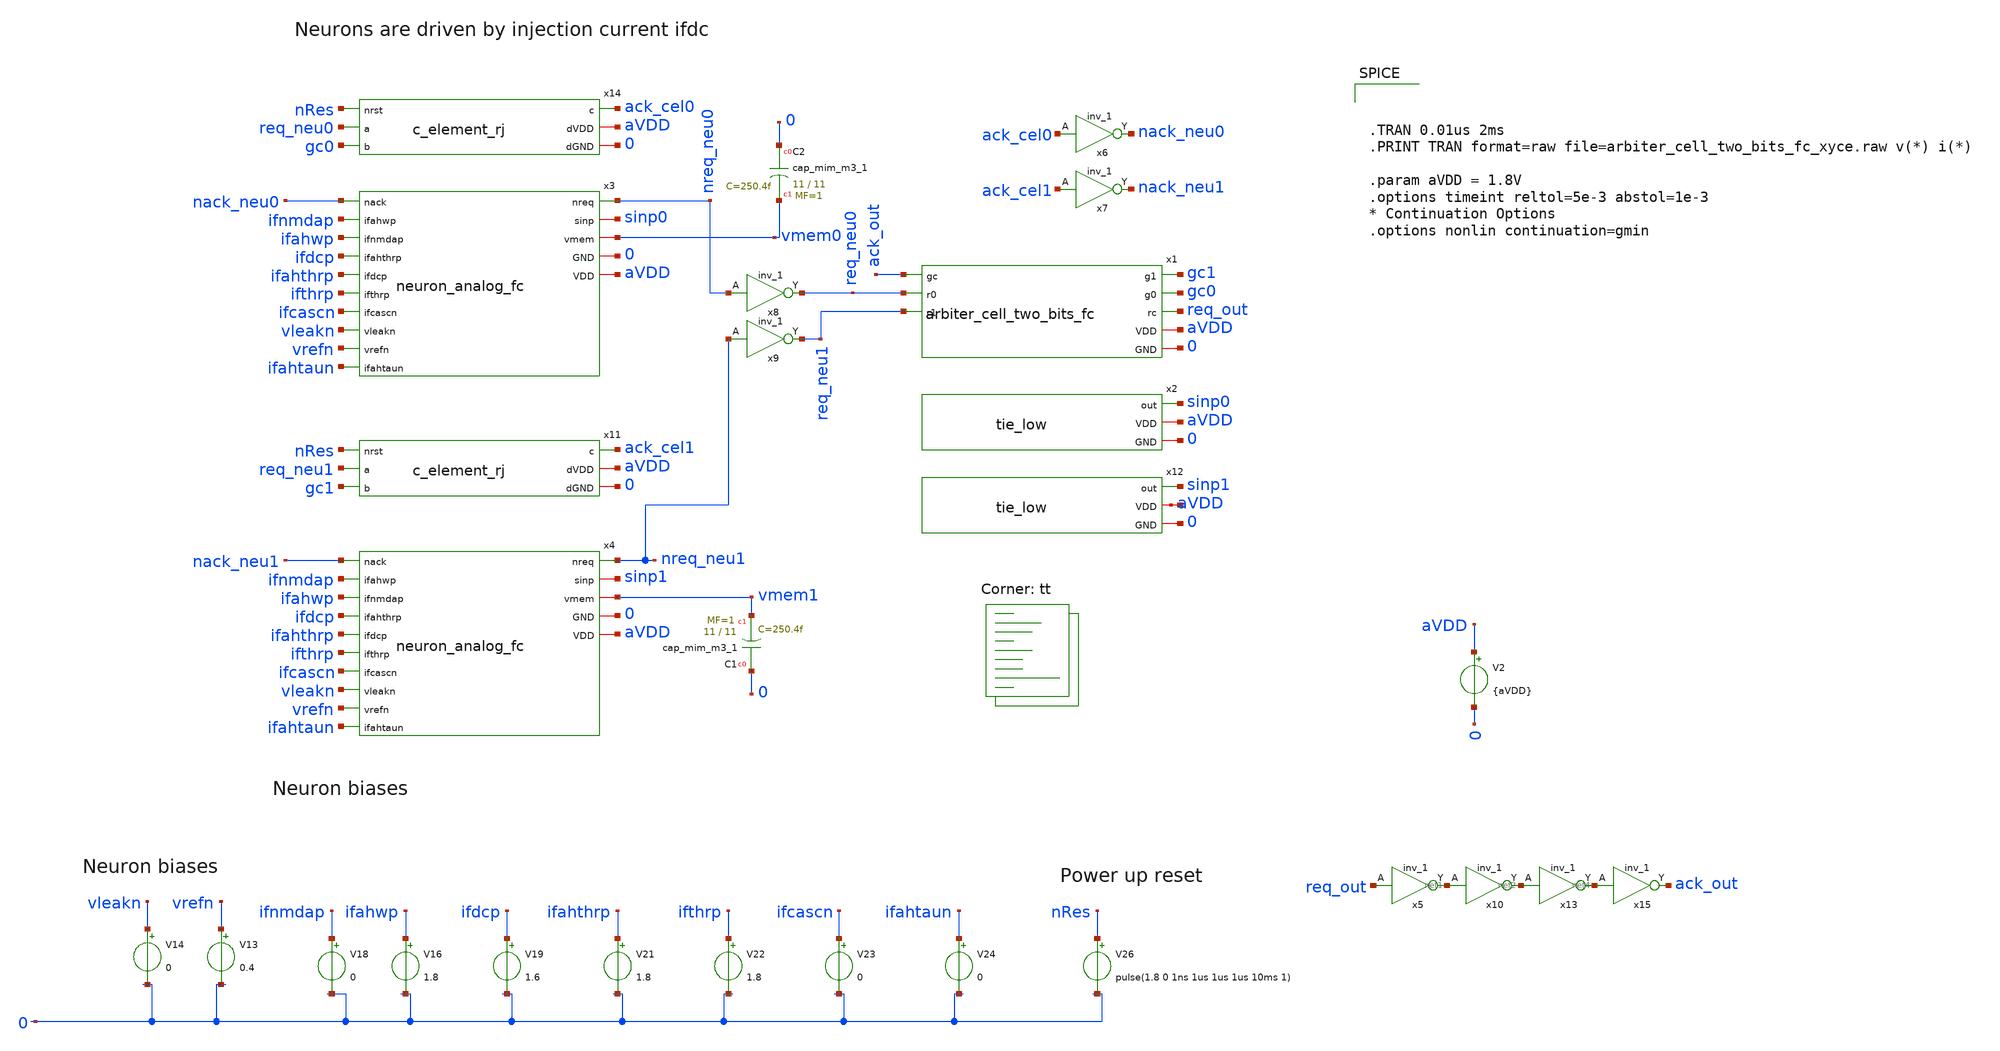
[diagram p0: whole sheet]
** sch_path: design/xschem/arbiter_cell_two_bits_fc_tb.sch
**.subckt arbiter_cell_two_bits_fc_tb
x1 gc1 gc0 ack_out req_out req_neu0 req_neu1 aVDD 0 arbiter_cell_two_bits_fc
V2 aVDD 0 {aVDD}
x3 nreq_neu0 sinp0 nack_neu0 ifnmdap ifahwp ifdcp vmem0 ifahthrp ifthrp ifcascn vleakn vrefn
+ ifahtaun 0 aVDD neuron_analog_fc
x4 nreq_neu1 sinp1 nack_neu1 ifnmdap ifahwp ifdcp vmem1 ifahthrp ifthrp ifcascn vleakn vrefn
+ ifahtaun 0 aVDD neuron_analog_fc
x6 ack_cel0 0 0 aVDD aVDD nack_neu0 sky130_fd_sc_hd__inv_1
x7 ack_cel1 0 0 aVDD aVDD nack_neu1 sky130_fd_sc_hd__inv_1
x8 nreq_neu0 0 0 aVDD aVDD req_neu0 sky130_fd_sc_hd__inv_1
x9 nreq_neu1 0 0 aVDD aVDD req_neu1 sky130_fd_sc_hd__inv_1
x5 req_out 0 0 aVDD aVDD net1 sky130_fd_sc_hd__inv_1
x10 net1 0 0 aVDD aVDD net2 sky130_fd_sc_hd__inv_1
x14 nRes req_neu0 gc0 ack_cel0 aVDD 0 c_element_rj
x11 nRes req_neu1 gc1 ack_cel1 aVDD 0 c_element_rj
XC1 0 vmem1 sky130_fd_pr__cap_mim_m3_1 W=11 L=11 MF=1 m=1
V13 vrefn 0 0.4
V14 vleakn 0 0
V16 ifahwp 0 1.8
V18 ifnmdap 0 0
V19 ifdcp 0 1.6
V21 ifahthrp 0 1.8
V22 ifthrp 0 1.8
V23 ifcascn 0 0
V24 ifahtaun 0 0
V26 nRes 0 pulse(1.8 0 1ns 1us 1us 1us 10ms 1)
XC2 0 vmem0 sky130_fd_pr__cap_mim_m3_1 W=11 L=11 MF=1 m=1
x2 sinp0 aVDD 0 tie_low
x12 sinp1 net3 0 tie_low
x13 net2 0 0 aVDD aVDD net4 sky130_fd_sc_hd__inv_1
x15 net4 0 0 aVDD aVDD ack_out sky130_fd_sc_hd__inv_1
**** begin user architecture code



.TRAN 0.01us 2ms
.PRINT TRAN format=raw file=arbiter_cell_two_bits_fc_xyce.raw v(*) i(*)

.param aVDD = 1.8V
.options timeint reltol=5e-3 abstol=1e-3
* Continuation Options
.options nonlin continuation=gmin





* Standard cell simulation files
.include $::SKYWATER_STDCELLS/sky130_fd_sc_hd.spice


.lib $::SKYWATER_MODELS/sky130.lib.spice tt
**** end user architecture code
**.ends

* expanding   symbol:  arbiter_cell_two_bits_fc.sym # of pins=8
** sym_path: design/xschem/arbiter_cell_two_bits_fc.sym
** sch_path: design/xschem/arbiter_cell_two_bits_fc.sch
.subckt arbiter_cell_two_bits_fc g1 g0 gc rc r0 r1 VDD GND
*.ipin r1
*.ipin r0
*.opin g0
*.opin g1
*.opin rc
*.ipin gc
*.iopin GND
*.iopin VDD
x1 net6 net5 GND GND VDD VDD net7 sky130_fd_sc_hd__nand2_1
x2 r0 gc GND GND VDD VDD net4 sky130_fd_sc_hd__or2_1
x3 net3 net1 GND GND VDD VDD g0 sky130_fd_sc_hd__nor2_1
x4 net6 net6 net6 net6 GND GND VDD VDD net3 sky130_fd_sc_hd__or4_1
x5 gc GND GND VDD VDD net1 sky130_fd_sc_hd__inv_1
x6 gc r1 GND GND VDD VDD net5 sky130_fd_sc_hd__or2_1
x7 net4 net7 GND GND VDD VDD net6 sky130_fd_sc_hd__nand2_1
x8 net7 net7 net7 net7 GND GND VDD VDD net2 sky130_fd_sc_hd__or4_1
x9 net1 net2 GND GND VDD VDD g1 sky130_fd_sc_hd__nor2_1
x10 net2 r0 GND GND VDD VDD net8 sky130_fd_sc_hd__nand2_1
x11 net3 r1 GND GND VDD VDD net9 sky130_fd_sc_hd__nand2_1
x12 net8 net9 GND GND VDD VDD rc sky130_fd_sc_hd__nand2_1
.ends


* expanding   symbol:  neuron_analog_fc.sym # of pins=15
** sym_path: design/xschem/neuron_analog_fc.sym
** sch_path: design/xschem/neuron_analog_fc.sch
.subckt neuron_analog_fc nreq sinp nack ifahwp ifnmdap ifahthrp vmem ifdcp ifthrp ifcascn vleakn
+ vrefn ifahtaun GND VDD
*.ipin vleakn
*.iopin GND
*.iopin VDD
*.opin nreq
*.ipin vrefn
*.ipin nack
*.ipin ifdcp
*.ipin ifthrp
*.ipin ifnmdap
*.ipin ifahwp
*.ipin ifahthrp
*.ipin ifahtaun
*.ipin ifcascn
*.iopin vmem
*.iopin sinp
XC1 GND vmem sky130_fd_pr__cap_mim_m3_1 W=11 L=11 MF=1 m=1
XM8 net4 vrefn GND GND sky130_fd_pr__nfet_01v8 L=0.25 W=0.8 nf=1 ad='int((nf+1)/2) * W/nf * 0.29' as='int((nf+2)/2) * W/nf * 0.29'
+ pd='2*int((nf+1)/2) * (W/nf + 0.29)' ps='2*int((nf+2)/2) * (W/nf + 0.29)' nrd='0.29 / W' nrs='0.29 / W'
+ sa=0 sb=0 sd=0 mult=1 m=1
XM9 net5 nack VDD VDD sky130_fd_pr__pfet_01v8 L=0.2 W=1.2 nf=1 ad='int((nf+1)/2) * W/nf * 0.29' as='int((nf+2)/2) * W/nf * 0.29'
+ pd='2*int((nf+1)/2) * (W/nf + 0.29)' ps='2*int((nf+2)/2) * (W/nf + 0.29)' nrd='0.29 / W' nrs='0.29 / W'
+ sa=0 sb=0 sd=0 mult=1 m=1
XC2 GND net3 sky130_fd_pr__cap_mim_m3_1 W=4 L=2 MF=1 m=1
XM21 vmem net3 GND GND sky130_fd_pr__nfet_01v8 L=0.25 W=1 nf=1 ad='int((nf+1)/2) * W/nf * 0.29' as='int((nf+2)/2) * W/nf * 0.29'
+ pd='2*int((nf+1)/2) * (W/nf + 0.29)' ps='2*int((nf+2)/2) * (W/nf + 0.29)' nrd='0.29 / W' nrs='0.29 / W'
+ sa=0 sb=0 sd=0 mult=1 m=1
XM15 net12 ifnmdap sinp VDD sky130_fd_pr__pfet_01v8 L=0.15 W=1 nf=1 ad='int((nf+1)/2) * W/nf * 0.29'
+ as='int((nf+2)/2) * W/nf * 0.29' pd='2*int((nf+1)/2) * (W/nf + 0.29)' ps='2*int((nf+2)/2) * (W/nf + 0.29)'
+ nrd='0.29 / W' nrs='0.29 / W' sa=0 sb=0 sd=0 mult=1 m=1
XC3 GND net8 sky130_fd_pr__cap_mim_m3_1 W=5 L=5 MF=1 m=1
XM12 GND vmem sinp VDD sky130_fd_pr__pfet_01v8 L=0.15 W=1 nf=1 ad='int((nf+1)/2) * W/nf * 0.29' as='int((nf+2)/2) * W/nf * 0.29'
+ pd='2*int((nf+1)/2) * (W/nf + 0.29)' ps='2*int((nf+2)/2) * (W/nf + 0.29)' nrd='0.29 / W' nrs='0.29 / W'
+ sa=0 sb=0 sd=0 mult=1 m=1
XM11 GND ifthrp net6 VDD sky130_fd_pr__pfet_01v8 L=0.15 W=1 nf=1 ad='int((nf+1)/2) * W/nf * 0.29' as='int((nf+2)/2) * W/nf * 0.29'
+ pd='2*int((nf+1)/2) * (W/nf + 0.29)' ps='2*int((nf+2)/2) * (W/nf + 0.29)' nrd='0.29 / W' nrs='0.29 / W'
+ sa=0 sb=0 sd=0 mult=1 m=1
XM16 net7 nack VDD VDD sky130_fd_pr__pfet_01v8 L=0.15 W=1 nf=1 ad='int((nf+1)/2) * W/nf * 0.29' as='int((nf+2)/2) * W/nf * 0.29'
+ pd='2*int((nf+1)/2) * (W/nf + 0.29)' ps='2*int((nf+2)/2) * (W/nf + 0.29)' nrd='0.29 / W' nrs='0.29 / W'
+ sa=0 sb=0 sd=0 mult=1 m=1
XM17 net9 ifahwp net7 VDD sky130_fd_pr__pfet_01v8 L=0.15 W=1 nf=1 ad='int((nf+1)/2) * W/nf * 0.29' as='int((nf+2)/2) * W/nf * 0.29'
+ pd='2*int((nf+1)/2) * (W/nf + 0.29)' ps='2*int((nf+2)/2) * (W/nf + 0.29)' nrd='0.29 / W' nrs='0.29 / W'
+ sa=0 sb=0 sd=0 mult=1 m=1
XM18 GND ifahthrp net9 VDD sky130_fd_pr__pfet_01v8 L=0.15 W=1 nf=1 ad='int((nf+1)/2) * W/nf * 0.29' as='int((nf+2)/2) * W/nf * 0.29'
+ pd='2*int((nf+1)/2) * (W/nf + 0.29)' ps='2*int((nf+2)/2) * (W/nf + 0.29)' nrd='0.29 / W' nrs='0.29 / W'
+ sa=0 sb=0 sd=0 mult=1 m=1
XM19 net8 net8 net9 VDD sky130_fd_pr__pfet_01v8 L=0.15 W=1 nf=1 ad='int((nf+1)/2) * W/nf * 0.29' as='int((nf+2)/2) * W/nf * 0.29'
+ pd='2*int((nf+1)/2) * (W/nf + 0.29)' ps='2*int((nf+2)/2) * (W/nf + 0.29)' nrd='0.29 / W' nrs='0.29 / W'
+ sa=0 sb=0 sd=0 mult=1 m=1
XM1 net11 ifdcp VDD VDD sky130_fd_pr__pfet_01v8 L=0.3 W=1 nf=1 ad='int((nf+1)/2) * W/nf * 0.29' as='int((nf+2)/2) * W/nf * 0.29'
+ pd='2*int((nf+1)/2) * (W/nf + 0.29)' ps='2*int((nf+2)/2) * (W/nf + 0.29)' nrd='0.29 / W' nrs='0.29 / W'
+ sa=0 sb=0 sd=0 mult=1 m=1
XM5 net2 nreq VDD VDD sky130_fd_pr__pfet_01v8 L=0.15 W=1 nf=1 ad='int((nf+1)/2) * W/nf * 0.29' as='int((nf+2)/2) * W/nf * 0.29'
+ pd='2*int((nf+1)/2) * (W/nf + 0.29)' ps='2*int((nf+2)/2) * (W/nf + 0.29)' nrd='0.29 / W' nrs='0.29 / W'
+ sa=0 sb=0 sd=0 mult=1 m=1
XM6 nreq vmem net2 VDD sky130_fd_pr__pfet_01v8 L=0.15 W=1 nf=1 ad='int((nf+1)/2) * W/nf * 0.29' as='int((nf+2)/2) * W/nf * 0.29'
+ pd='2*int((nf+1)/2) * (W/nf + 0.29)' ps='2*int((nf+2)/2) * (W/nf + 0.29)' nrd='0.29 / W' nrs='0.29 / W'
+ sa=0 sb=0 sd=0 mult=1 m=1
XM10 net3 nreq net5 VDD sky130_fd_pr__pfet_01v8 L=0.15 W=1 nf=1 ad='int((nf+1)/2) * W/nf * 0.29' as='int((nf+2)/2) * W/nf * 0.29'
+ pd='2*int((nf+1)/2) * (W/nf + 0.29)' ps='2*int((nf+2)/2) * (W/nf + 0.29)' nrd='0.29 / W' nrs='0.29 / W'
+ sa=0 sb=0 sd=0 mult=1 m=1
XM2 nreq vmem net1 GND sky130_fd_pr__nfet_01v8 L=0.15 W=0.65 nf=1 ad='int((nf+1)/2) * W/nf * 0.29' as='int((nf+2)/2) * W/nf * 0.29'
+ pd='2*int((nf+1)/2) * (W/nf + 0.29)' ps='2*int((nf+2)/2) * (W/nf + 0.29)' nrd='0.29 / W' nrs='0.29 / W'
+ sa=0 sb=0 sd=0 mult=1 m=1
XM3 net1 net1 GND GND sky130_fd_pr__nfet_01v8 L=0.15 W=0.65 nf=1 ad='int((nf+1)/2) * W/nf * 0.29' as='int((nf+2)/2) * W/nf * 0.29'
+ pd='2*int((nf+1)/2) * (W/nf + 0.29)' ps='2*int((nf+2)/2) * (W/nf + 0.29)' nrd='0.29 / W' nrs='0.29 / W'
+ sa=0 sb=0 sd=0 mult=1 m=1
XM7 net3 nreq net4 GND sky130_fd_pr__nfet_01v8 L=0.15 W=0.65 nf=1 ad='int((nf+1)/2) * W/nf * 0.29' as='int((nf+2)/2) * W/nf * 0.29'
+ pd='2*int((nf+1)/2) * (W/nf + 0.29)' ps='2*int((nf+2)/2) * (W/nf + 0.29)' nrd='0.29 / W' nrs='0.29 / W'
+ sa=0 sb=0 sd=0 mult=1 m=1
XM14 vmem vleakn net13 GND sky130_fd_pr__nfet_01v8 L=0.15 W=0.65 nf=1 ad='int((nf+1)/2) * W/nf * 0.29'
+ as='int((nf+2)/2) * W/nf * 0.29' pd='2*int((nf+1)/2) * (W/nf + 0.29)' ps='2*int((nf+2)/2) * (W/nf + 0.29)'
+ nrd='0.29 / W' nrs='0.29 / W' sa=0 sb=0 sd=0 mult=1 m=1
XM4 vmem nreq VDD VDD sky130_fd_pr__pfet_01v8 L=0.15 W=1 nf=1 ad='int((nf+1)/2) * W/nf * 0.29' as='int((nf+2)/2) * W/nf * 0.29'
+ pd='2*int((nf+1)/2) * (W/nf + 0.29)' ps='2*int((nf+2)/2) * (W/nf + 0.29)' nrd='0.29 / W' nrs='0.29 / W'
+ sa=0 sb=0 sd=0 mult=1 m=1
XM24 vmem vmem net6 VDD sky130_fd_pr__pfet_01v8 L=0.15 W=1 nf=1 ad='int((nf+1)/2) * W/nf * 0.29' as='int((nf+2)/2) * W/nf * 0.29'
+ pd='2*int((nf+1)/2) * (W/nf + 0.29)' ps='2*int((nf+2)/2) * (W/nf + 0.29)' nrd='0.29 / W' nrs='0.29 / W'
+ sa=0 sb=0 sd=0 mult=1 m=1
Vmeas net11 net6 0
.save i(vmeas)
Vmeas1 net13 GND 0
.save i(vmeas1)
XM13 net6 ifcascn net10 GND sky130_fd_pr__nfet_01v8 L=0.15 W=0.65 nf=1 ad='int((nf+1)/2) * W/nf * 0.29'
+ as='int((nf+2)/2) * W/nf * 0.29' pd='2*int((nf+1)/2) * (W/nf + 0.29)' ps='2*int((nf+2)/2) * (W/nf + 0.29)'
+ nrd='0.29 / W' nrs='0.29 / W' sa=0 sb=0 sd=0 mult=1 m=1
XM20 net10 net8 GND GND sky130_fd_pr__nfet_01v8 L=0.15 W=0.65 nf=1 ad='int((nf+1)/2) * W/nf * 0.29' as='int((nf+2)/2) * W/nf * 0.29'
+ pd='2*int((nf+1)/2) * (W/nf + 0.29)' ps='2*int((nf+2)/2) * (W/nf + 0.29)' nrd='0.29 / W' nrs='0.29 / W'
+ sa=0 sb=0 sd=0 mult=1 m=1
XM22 net8 ifahtaun GND GND sky130_fd_pr__nfet_01v8 L=0.15 W=0.65 nf=1 ad='int((nf+1)/2) * W/nf * 0.29'
+ as='int((nf+2)/2) * W/nf * 0.29' pd='2*int((nf+1)/2) * (W/nf + 0.29)' ps='2*int((nf+2)/2) * (W/nf + 0.29)'
+ nrd='0.29 / W' nrs='0.29 / W' sa=0 sb=0 sd=0 mult=1 m=1
.ends


* expanding   symbol:  c_element_rj.sym # of pins=6
** sym_path: design/xschem/c_element_rj.sym
** sch_path: design/xschem/c_element_rj.sch
.subckt c_element_rj nrst a b c dVDD dGND
*.iopin dGND
*.iopin dVDD
*.opin c
*.ipin b
*.ipin a
*.ipin nrst
XM14 c net6 dVDD dVDD sky130_fd_pr__pfet_01v8 L=0.15 W=1 nf=1 ad='int((nf+1)/2) * W/nf * 0.29' as='int((nf+2)/2) * W/nf * 0.29'
+ pd='2*int((nf+1)/2) * (W/nf + 0.29)' ps='2*int((nf+2)/2) * (W/nf + 0.29)' nrd='0.29 / W' nrs='0.29 / W'
+ sa=0 sb=0 sd=0 mult=1 m=1
XM5 net6 nrst dVDD dVDD sky130_fd_pr__pfet_01v8 L=0.15 W=1 nf=1 ad='int((nf+1)/2) * W/nf * 0.29' as='int((nf+2)/2) * W/nf * 0.29'
+ pd='2*int((nf+1)/2) * (W/nf + 0.29)' ps='2*int((nf+2)/2) * (W/nf + 0.29)' nrd='0.29 / W' nrs='0.29 / W'
+ sa=0 sb=0 sd=0 mult=1 m=1
XM6 net5 b dVDD dVDD sky130_fd_pr__pfet_01v8 L=0.15 W=1 nf=1 ad='int((nf+1)/2) * W/nf * 0.29' as='int((nf+2)/2) * W/nf * 0.29'
+ pd='2*int((nf+1)/2) * (W/nf + 0.29)' ps='2*int((nf+2)/2) * (W/nf + 0.29)' nrd='0.29 / W' nrs='0.29 / W'
+ sa=0 sb=0 sd=0 mult=1 m=1
XM4 net4 a dVDD dVDD sky130_fd_pr__pfet_01v8 L=0.15 W=1 nf=1 ad='int((nf+1)/2) * W/nf * 0.29' as='int((nf+2)/2) * W/nf * 0.29'
+ pd='2*int((nf+1)/2) * (W/nf + 0.29)' ps='2*int((nf+2)/2) * (W/nf + 0.29)' nrd='0.29 / W' nrs='0.29 / W'
+ sa=0 sb=0 sd=0 mult=1 m=1
XM7 net3 b net4 dVDD sky130_fd_pr__pfet_01v8 L=0.15 W=1 nf=1 ad='int((nf+1)/2) * W/nf * 0.29' as='int((nf+2)/2) * W/nf * 0.29'
+ pd='2*int((nf+1)/2) * (W/nf + 0.29)' ps='2*int((nf+2)/2) * (W/nf + 0.29)' nrd='0.29 / W' nrs='0.29 / W'
+ sa=0 sb=0 sd=0 mult=1 m=1
XM8 net3 a net5 dVDD sky130_fd_pr__pfet_01v8 L=0.15 W=1 nf=1 ad='int((nf+1)/2) * W/nf * 0.29' as='int((nf+2)/2) * W/nf * 0.29'
+ pd='2*int((nf+1)/2) * (W/nf + 0.29)' ps='2*int((nf+2)/2) * (W/nf + 0.29)' nrd='0.29 / W' nrs='0.29 / W'
+ sa=0 sb=0 sd=0 mult=1 m=1
XM10 net5 c net4 dVDD sky130_fd_pr__pfet_01v8 L=0.15 W=1 nf=1 ad='int((nf+1)/2) * W/nf * 0.29' as='int((nf+2)/2) * W/nf * 0.29'
+ pd='2*int((nf+1)/2) * (W/nf + 0.29)' ps='2*int((nf+2)/2) * (W/nf + 0.29)' nrd='0.29 / W' nrs='0.29 / W'
+ sa=0 sb=0 sd=0 mult=1 m=1
XM12 c net6 dGND dGND sky130_fd_pr__nfet_01v8 L=0.15 W=0.65 nf=1 ad='int((nf+1)/2) * W/nf * 0.29' as='int((nf+2)/2) * W/nf * 0.29'
+ pd='2*int((nf+1)/2) * (W/nf + 0.29)' ps='2*int((nf+2)/2) * (W/nf + 0.29)' nrd='0.29 / W' nrs='0.29 / W'
+ sa=0 sb=0 sd=0 mult=1 m=1
XM1 net3 nrst net6 dGND sky130_fd_pr__nfet_01v8 L=0.15 W=0.65 nf=1 ad='int((nf+1)/2) * W/nf * 0.29' as='int((nf+2)/2) * W/nf * 0.29'
+ pd='2*int((nf+1)/2) * (W/nf + 0.29)' ps='2*int((nf+2)/2) * (W/nf + 0.29)' nrd='0.29 / W' nrs='0.29 / W'
+ sa=0 sb=0 sd=0 mult=1 m=1
XM2 net3 b net1 dGND sky130_fd_pr__nfet_01v8 L=0.15 W=0.65 nf=1 ad='int((nf+1)/2) * W/nf * 0.29' as='int((nf+2)/2) * W/nf * 0.29'
+ pd='2*int((nf+1)/2) * (W/nf + 0.29)' ps='2*int((nf+2)/2) * (W/nf + 0.29)' nrd='0.29 / W' nrs='0.29 / W'
+ sa=0 sb=0 sd=0 mult=1 m=1
XM3 net3 a net2 dGND sky130_fd_pr__nfet_01v8 L=0.15 W=0.65 nf=1 ad='int((nf+1)/2) * W/nf * 0.29' as='int((nf+2)/2) * W/nf * 0.29'
+ pd='2*int((nf+1)/2) * (W/nf + 0.29)' ps='2*int((nf+2)/2) * (W/nf + 0.29)' nrd='0.29 / W' nrs='0.29 / W'
+ sa=0 sb=0 sd=0 mult=1 m=1
XM9 net2 c net1 dGND sky130_fd_pr__nfet_01v8 L=0.15 W=0.65 nf=1 ad='int((nf+1)/2) * W/nf * 0.29' as='int((nf+2)/2) * W/nf * 0.29'
+ pd='2*int((nf+1)/2) * (W/nf + 0.29)' ps='2*int((nf+2)/2) * (W/nf + 0.29)' nrd='0.29 / W' nrs='0.29 / W'
+ sa=0 sb=0 sd=0 mult=1 m=1
XM11 net1 a dGND dGND sky130_fd_pr__nfet_01v8 L=0.15 W=0.65 nf=1 ad='int((nf+1)/2) * W/nf * 0.29' as='int((nf+2)/2) * W/nf * 0.29'
+ pd='2*int((nf+1)/2) * (W/nf + 0.29)' ps='2*int((nf+2)/2) * (W/nf + 0.29)' nrd='0.29 / W' nrs='0.29 / W'
+ sa=0 sb=0 sd=0 mult=1 m=1
XM13 net2 b dGND dGND sky130_fd_pr__nfet_01v8 L=0.15 W=0.65 nf=1 ad='int((nf+1)/2) * W/nf * 0.29' as='int((nf+2)/2) * W/nf * 0.29'
+ pd='2*int((nf+1)/2) * (W/nf + 0.29)' ps='2*int((nf+2)/2) * (W/nf + 0.29)' nrd='0.29 / W' nrs='0.29 / W'
+ sa=0 sb=0 sd=0 mult=1 m=1
.ends


* expanding   symbol:  tie_low.sym # of pins=3
** sym_path: design/xschem/tie_low.sym
** sch_path: design/xschem/tie_low.sch
.subckt tie_low out VDD GND
*.iopin VDD
*.iopin GND
*.opin out
XM4 net1 net1 VDD VDD sky130_fd_pr__pfet_01v8 L=0.15 W=1 nf=1 ad='int((nf+1)/2) * W/nf * 0.29' as='int((nf+2)/2) * W/nf * 0.29'
+ pd='2*int((nf+1)/2) * (W/nf + 0.29)' ps='2*int((nf+2)/2) * (W/nf + 0.29)' nrd='0.29 / W' nrs='0.29 / W'
+ sa=0 sb=0 sd=0 mult=1 m=1
XM2 out net1 GND GND sky130_fd_pr__nfet_01v8 L=0.15 W=0.65 nf=1 ad='int((nf+1)/2) * W/nf * 0.29' as='int((nf+2)/2) * W/nf * 0.29'
+ pd='2*int((nf+1)/2) * (W/nf + 0.29)' ps='2*int((nf+2)/2) * (W/nf + 0.29)' nrd='0.29 / W' nrs='0.29 / W'
+ sa=0 sb=0 sd=0 mult=1 m=1
.ends

.end
